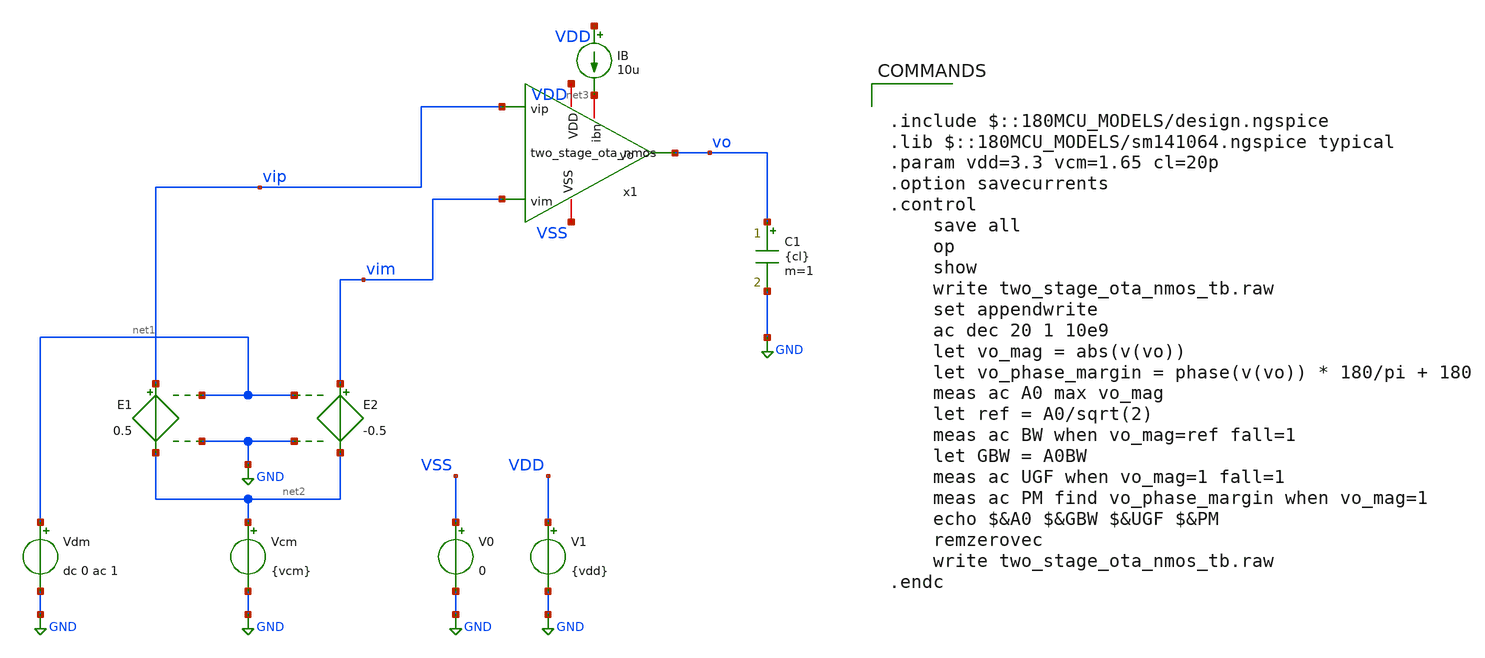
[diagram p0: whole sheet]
** sch_path: DESIGN/DACFUTURE_EDU/Two_stage_OTA/two_stage_ota_nmos_tb.sch
**.subckt two_stage_ota_nmos_tb
E1 vip net2 net1 GND 0.5
E2 vim net2 net1 GND -0.5
Vdm net1 GND dc 0 ac 1
Vcm net2 GND {vcm}
V0 VSS GND 0
V1 VDD GND {vdd}
C1 vo GND {cl} m=1
IB VDD net3 10u
x1 vip vim vo VDD VSS net3 two_stage_ota_nmos
**** begin user architecture code

.include $::180MCU_MODELS/design.ngspice
.lib $::180MCU_MODELS/sm141064.ngspice typical
.param vdd=3.3 vcm=1.65 cl=20p
.option savecurrents
.control
    save all
    op
    show
    write two_stage_ota_nmos_tb.raw
    set appendwrite
    ac dec 20 1 10e9
    let vo_mag = abs(v(vo))
    let vo_phase_margin = phase(v(vo)) * 180/pi + 180
    meas ac A0 max vo_mag
    let ref = A0/sqrt(2)
    meas ac BW when vo_mag=ref fall=1
    let GBW = A0BW
    meas ac UGF when vo_mag=1 fall=1
    meas ac PM find vo_phase_margin when vo_mag=1
    echo $&A0 $&GBW $&UGF $&PM
    remzerovec
    write two_stage_ota_nmos_tb.raw
.endc



**** end user architecture code
**.ends

* expanding   symbol:  DACFUTURE_EDU/Two_stage_OTA/two_stage_ota_nmos.sym # of pins=6
** sym_path: DESIGN/DACFUTURE_EDU/Two_stage_OTA/two_stage_ota_nmos.sym
** sch_path: DESIGN/DACFUTURE_EDU/Two_stage_OTA/two_stage_ota_nmos.sch
.subckt two_stage_ota_nmos vip vim vo VDD VSS ibn
*.ipin vip
*.ipin vim
*.opin vo
*.iopin VDD
*.iopin VSS
*.iopin ibn
XM2b vofirst vmirr VDD VDD pfet_03v3 L=2u W=31.45u nf=7 ad='int((nf+1)/2) * W/nf * 0.18u' as='int((nf+2)/2) * W/nf * 0.18u'
+ pd='2*int((nf+1)/2) * (W/nf + 0.18u)' ps='2*int((nf+2)/2) * (W/nf + 0.18u)' nrd='0.18u / W' nrs='0.18u / W'
+ sa=0 sb=0 sd=0 m=1
XM2a vmirr vmirr VDD VDD pfet_03v3 L=2u W=31.45u nf=7 ad='int((nf+1)/2) * W/nf * 0.18u' as='int((nf+2)/2) * W/nf * 0.18u'
+ pd='2*int((nf+1)/2) * (W/nf + 0.18u)' ps='2*int((nf+2)/2) * (W/nf + 0.18u)' nrd='0.18u / W' nrs='0.18u / W'
+ sa=0 sb=0 sd=0 m=1
XM1a vmirr vip vtail VSS nfet_03v3 L=1u W=3.34u nf=1 ad='int((nf+1)/2) * W/nf * 0.18u' as='int((nf+2)/2) * W/nf * 0.18u'
+ pd='2*int((nf+1)/2) * (W/nf + 0.18u)' ps='2*int((nf+2)/2) * (W/nf + 0.18u)' nrd='0.18u / W' nrs='0.18u / W'
+ sa=0 sb=0 sd=0 m=1
XM0b vtail ibn VSS VSS nfet_03v3 L=0.5u W=3.4u nf=1 ad='int((nf+1)/2) * W/nf * 0.18u' as='int((nf+2)/2) * W/nf * 0.18u'
+ pd='2*int((nf+1)/2) * (W/nf + 0.18u)' ps='2*int((nf+2)/2) * (W/nf + 0.18u)' nrd='0.18u / W' nrs='0.18u / W'
+ sa=0 sb=0 sd=0 m=1
XM1b vofirst vim vtail VSS nfet_03v3 L=1u W=3.34u nf=1 ad='int((nf+1)/2) * W/nf * 0.18u' as='int((nf+2)/2) * W/nf * 0.18u'
+ pd='2*int((nf+1)/2) * (W/nf + 0.18u)' ps='2*int((nf+2)/2) * (W/nf + 0.18u)' nrd='0.18u / W' nrs='0.18u / W'
+ sa=0 sb=0 sd=0 m=1
XM0a ibn ibn VSS VSS nfet_03v3 L=0.5u W=1.7u nf=1 ad='int((nf+1)/2) * W/nf * 0.18u' as='int((nf+2)/2) * W/nf * 0.18u'
+ pd='2*int((nf+1)/2) * (W/nf + 0.18u)' ps='2*int((nf+2)/2) * (W/nf + 0.18u)' nrd='0.18u / W' nrs='0.18u / W'
+ sa=0 sb=0 sd=0 m=1
XM4 vo ibn VSS VSS nfet_03v3 L=1u W=20.3u nf=5 ad='int((nf+1)/2) * W/nf * 0.18u' as='int((nf+2)/2) * W/nf * 0.18u'
+ pd='2*int((nf+1)/2) * (W/nf + 0.18u)' ps='2*int((nf+2)/2) * (W/nf + 0.18u)' nrd='0.18u / W' nrs='0.18u / W'
+ sa=0 sb=0 sd=0 m=1
XM3 vo vofirst VDD VDD pfet_03v3 L=0.5u W=44.2u nf=9 ad='int((nf+1)/2) * W/nf * 0.18u' as='int((nf+2)/2) * W/nf * 0.18u'
+ pd='2*int((nf+1)/2) * (W/nf + 0.18u)' ps='2*int((nf+2)/2) * (W/nf + 0.18u)' nrd='0.18u / W' nrs='0.18u / W'
+ sa=0 sb=0 sd=0 m=1
C1 vo vofirst 4.4p m=1
.ends

.GLOBAL GND
.end
